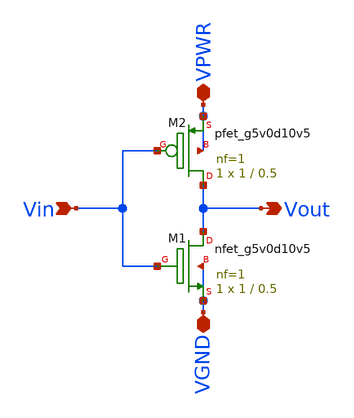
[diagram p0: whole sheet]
** sch_path: my_inv_1.sch
**.subckt my_inv_1 VGND VPWR Vin Vout
*.iopin VGND
*.iopin VPWR
*.ipin Vin
*.opin Vout
XM1 Vout Vin VGND VGND sky130_fd_pr__nfet_g5v0d10v5 L=0.5 W=1 nf=1 ad='int((nf+1)/2) * W/nf * 0.29' as='int((nf+2)/2) * W/nf * 0.29'
+ pd='2*int((nf+1)/2) * (W/nf + 0.29)' ps='2*int((nf+2)/2) * (W/nf + 0.29)' nrd='0.29 / W' nrs='0.29 / W'
+ sa=0 sb=0 sd=0 mult=1 m=1
XM2 Vout Vin VPWR VPWR sky130_fd_pr__pfet_g5v0d10v5 L=0.5 W=1 nf=1 ad='int((nf+1)/2) * W/nf * 0.29' as='int((nf+2)/2) * W/nf * 0.29'
+ pd='2*int((nf+1)/2) * (W/nf + 0.29)' ps='2*int((nf+2)/2) * (W/nf + 0.29)' nrd='0.29 / W' nrs='0.29 / W'
+ sa=0 sb=0 sd=0 mult=1 m=1
**.ends
.end
